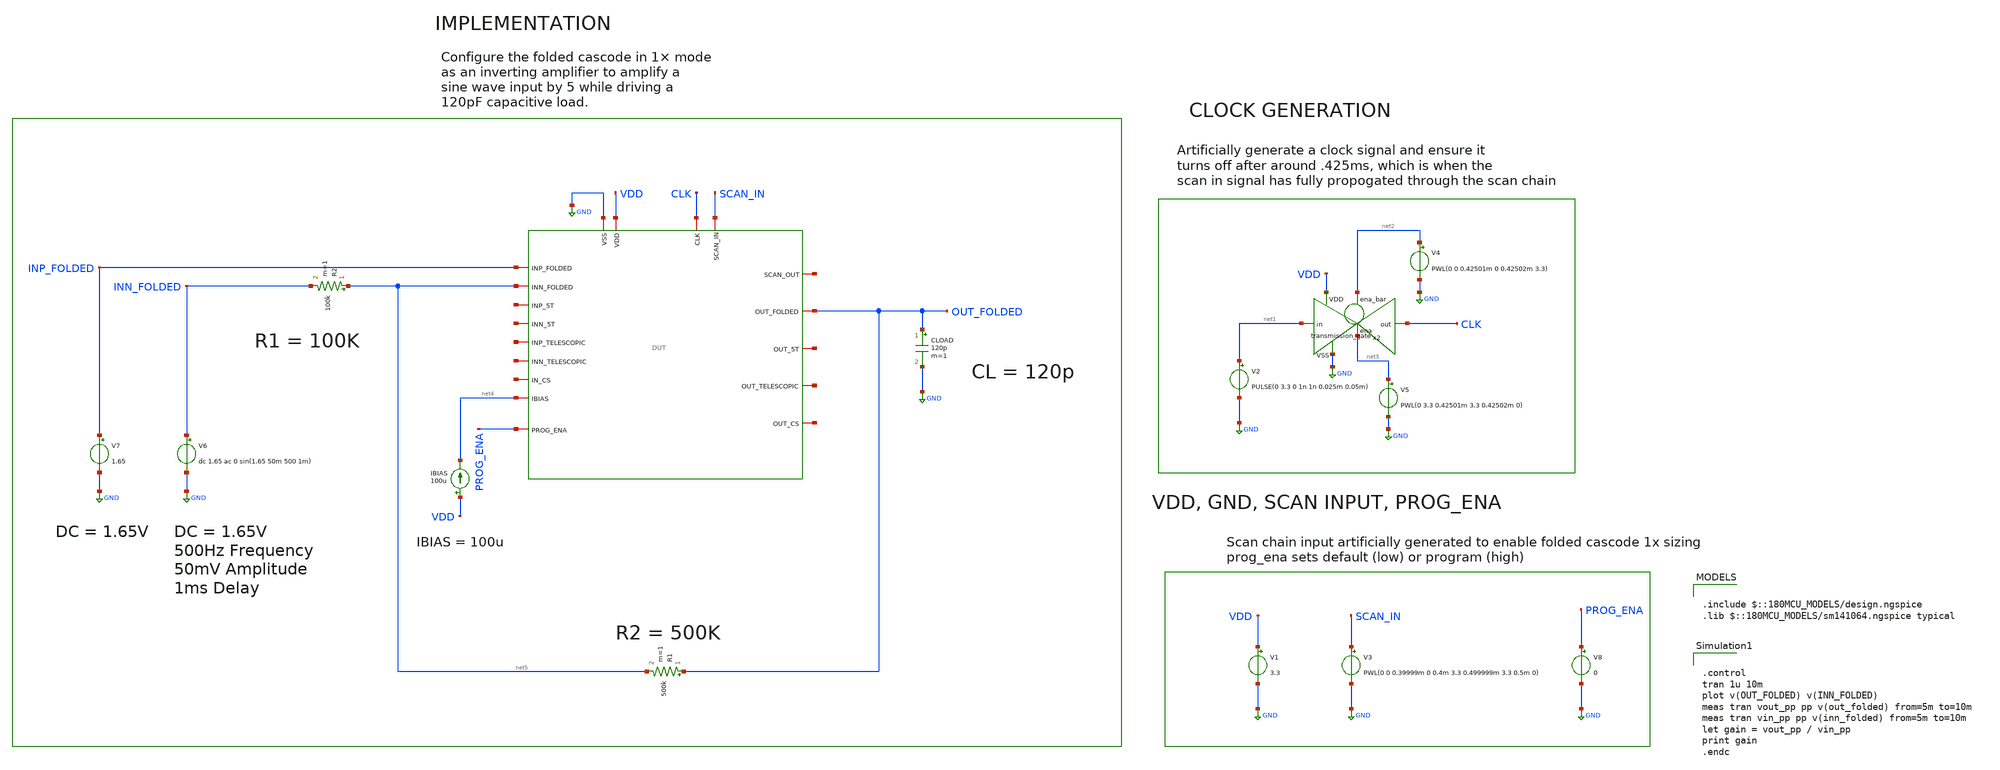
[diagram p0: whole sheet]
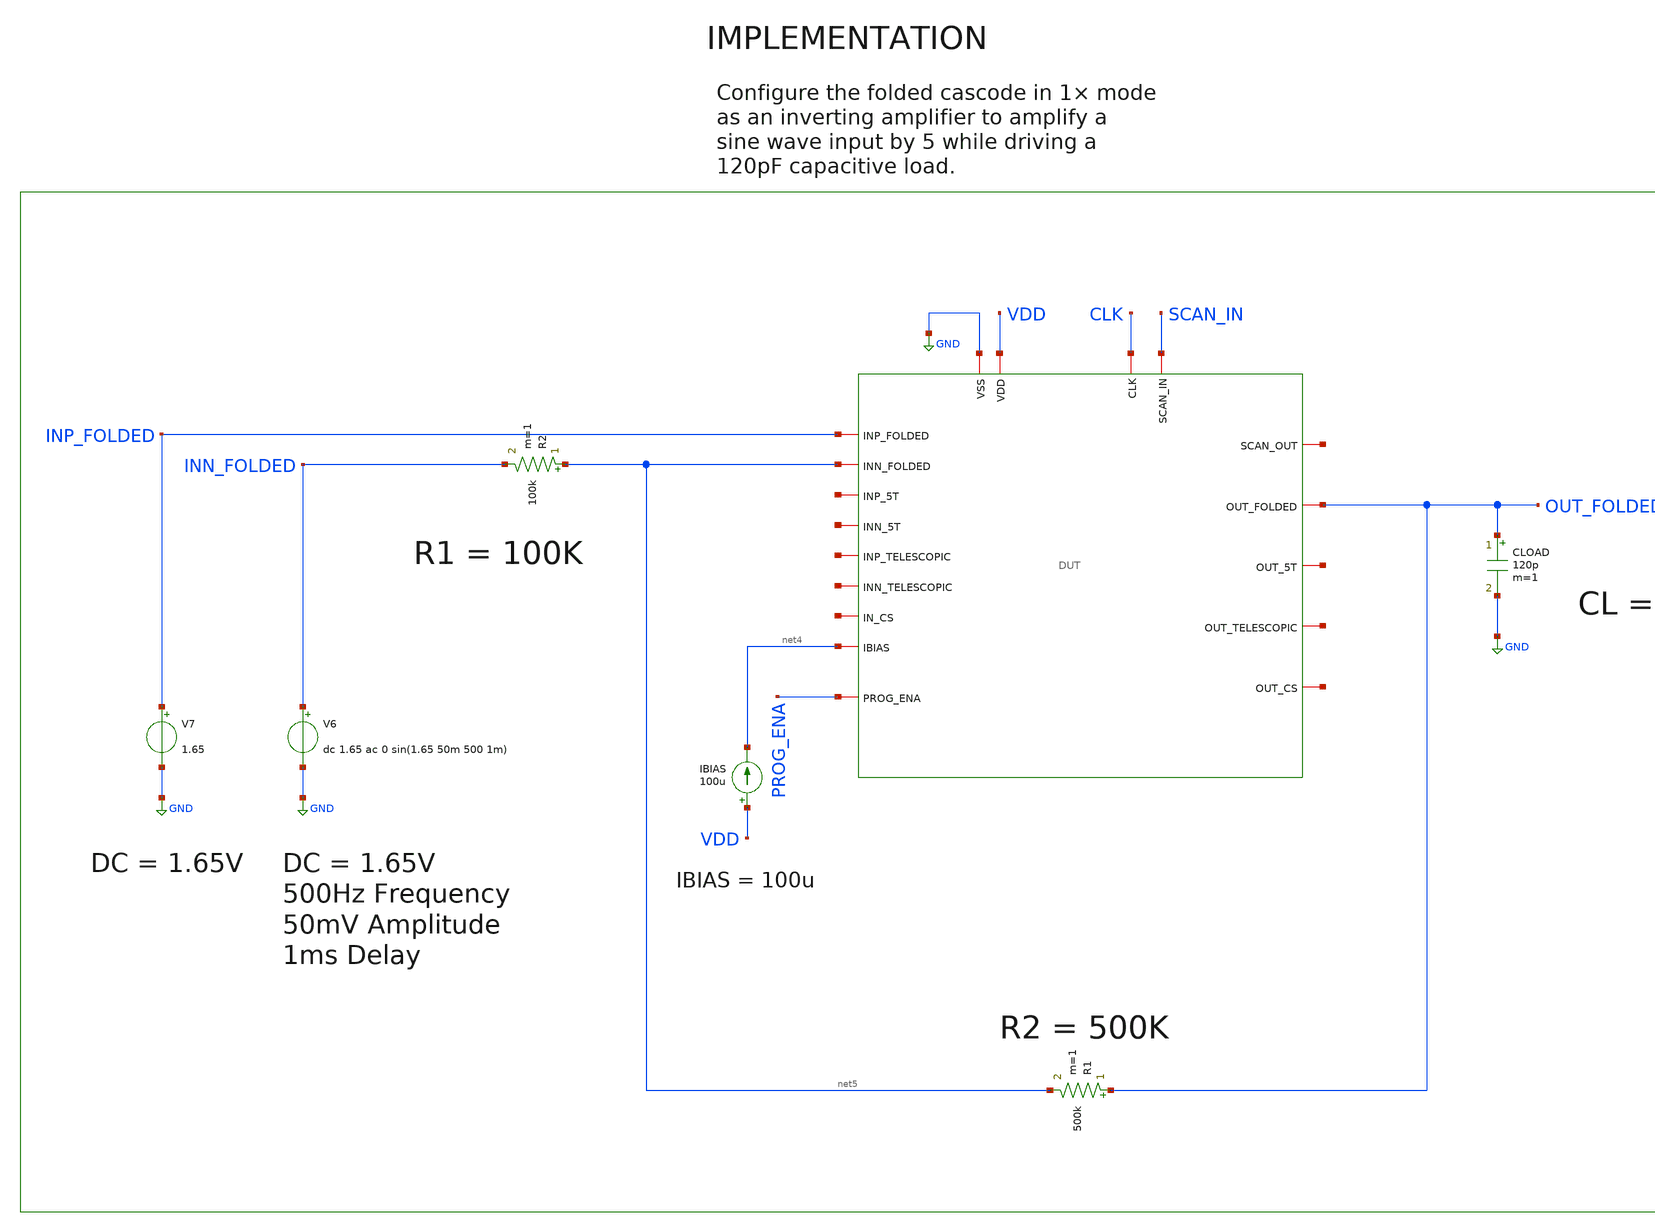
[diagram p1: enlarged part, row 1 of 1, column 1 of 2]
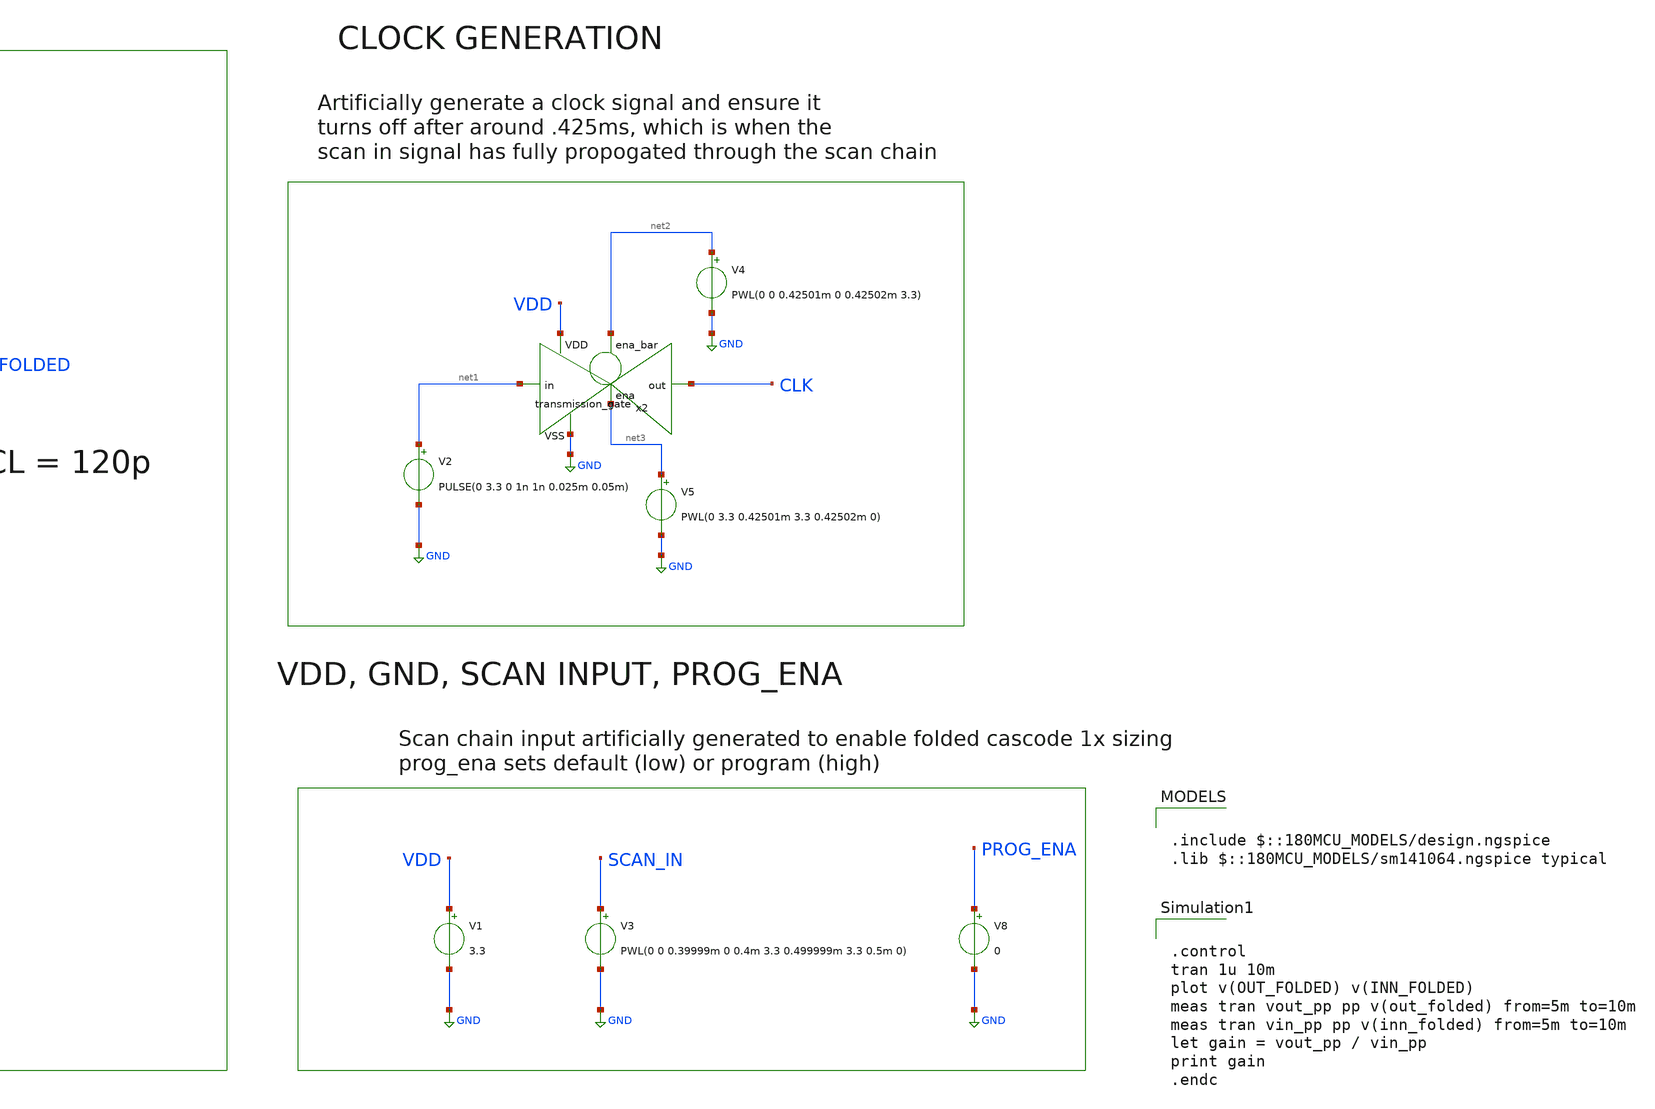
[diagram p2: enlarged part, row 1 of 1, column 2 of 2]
** sch_path: designs/libs/old_files/old_top_level/etj/ota_folded/inverting_amp/input_sine_1x.sch
**.subckt input_sine_1x
V3 SCAN_IN GND PWL(0 0 0.39999m 0 0.4m 3.3 0.499999m 3.3 0.5m 0)
V1 VDD GND 3.3
V2 net1 GND PULSE(0 3.3 0 1n 1n 0.025m 0.05m)
x2 net2 VDD CLK net1 GND net3 transmission_gate
V4 net2 GND PWL(0 0 0.42501m 0 0.42502m 3.3)
V5 net3 GND PWL(0 3.3 0.42501m 3.3 0.42502m 0)
IBIAS VDD net4 100u
V7 INP_FOLDED GND 1.65
CLOAD OUT_FOLDED GND 120p m=1
R2 net5 INN_FOLDED 100k m=1
V6 INN_FOLDED GND dc 1.65 ac 0 sin(1.65 50m 500 1m)
R1 OUT_FOLDED net5 500k m=1
x1 CLK net6 SCAN_IN GND VDD OUT_FOLDED INP_FOLDED net7 net4 net5 net8 net9 net10 net11 net12 net13
+ net14 PROG_ENA DUT
V8 PROG_ENA GND 0
**** begin user architecture code

.include $::180MCU_MODELS/design.ngspice
.lib $::180MCU_MODELS/sm141064.ngspice typical



.control
tran 1u 10m
plot v(OUT_FOLDED) v(INN_FOLDED)
meas tran vout_pp pp v(out_folded) from=5m to=10m
meas tran vin_pp pp v(inn_folded) from=5m to=10m
let gain = vout_pp / vin_pp
print gain
.endc


**** end user architecture code
**.ends
.GLOBAL GND
.end
